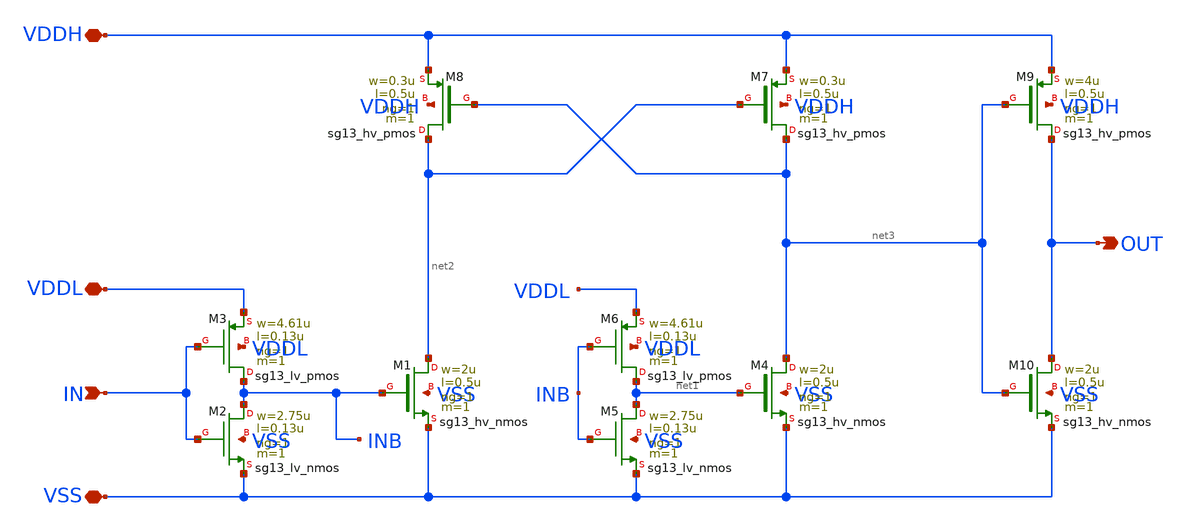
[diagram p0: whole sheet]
** sch_path: ip/util/xschem/levelup.sch
**.subckt levelup VSS VDDL IN VDDH OUT
*.iopin VSS
*.iopin VDDL
*.ipin IN
*.iopin VDDH
*.opin OUT
XM1 net2 INB VSS VSS sg13_hv_nmos w=2u l=0.5u ng=1 m=1 mm_ok=1
XM2 INB IN VSS VSS sg13_lv_nmos w=2.75u l=0.13u ng=1 m=1 mm_ok=1
XM3 INB IN VDDL VDDL sg13_lv_pmos w=4.61u l=0.13u ng=1 m=1 mm_ok=1
XM4 net3 net1 VSS VSS sg13_hv_nmos w=2u l=0.5u ng=1 m=1 mm_ok=1
XM5 net1 INB VSS VSS sg13_lv_nmos w=2.75u l=0.13u ng=1 m=1 mm_ok=1
XM6 net1 INB VDDL VDDL sg13_lv_pmos w=4.61u l=0.13u ng=1 m=1 mm_ok=1
XM7 net3 net2 VDDH VDDH sg13_hv_pmos w=0.3u l=0.5u ng=1 m=1 mm_ok=1
XM8 net2 net3 VDDH VDDH sg13_hv_pmos w=0.3u l=0.5u ng=1 m=1 mm_ok=1
XM9 OUT net3 VDDH VDDH sg13_hv_pmos w=4u l=0.5u ng=1 m=1 mm_ok=1
XM10 OUT net3 VSS VSS sg13_hv_nmos w=2u l=0.5u ng=1 m=1 mm_ok=1
**.ends
.end
